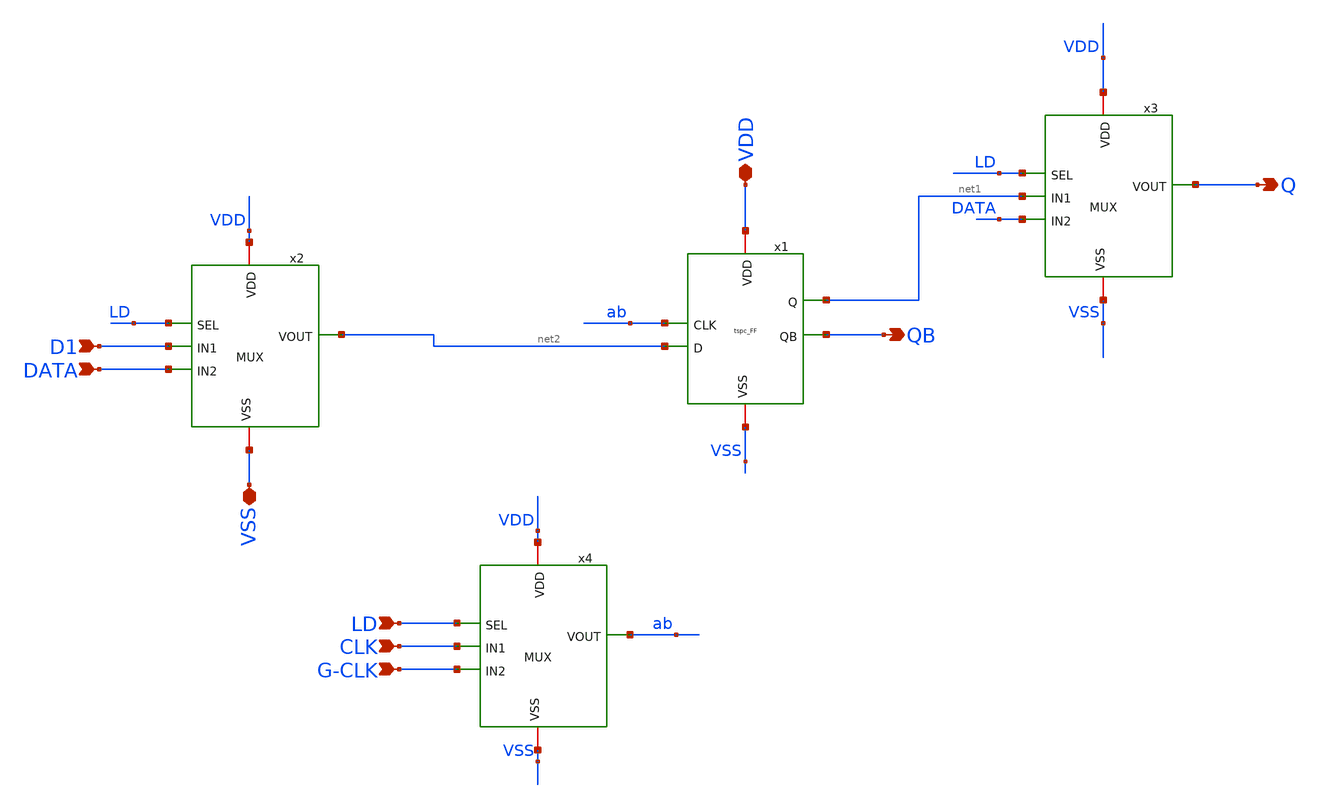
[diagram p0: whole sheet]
** sch_path: Xschem/PLL_TOP_Schematics/MOD_DFF_latest.sch
**.subckt MOD_DFF_latest VDD LD VSS D1 CLK G-CLK Q QB DATA
*.iopin VDD
*.ipin LD
*.iopin VSS
*.ipin D1
*.ipin CLK
*.ipin G-CLK
*.opin Q
*.opin QB
*.ipin DATA
x1 VDD QB net1 ab net2 VSS tspc_FF
x2 VDD LD D1 net2 VSS DATA MUX
x3 VDD LD net1 Q VSS DATA MUX
x4 VDD LD CLK ab VSS G-CLK MUX
**.ends
.end
